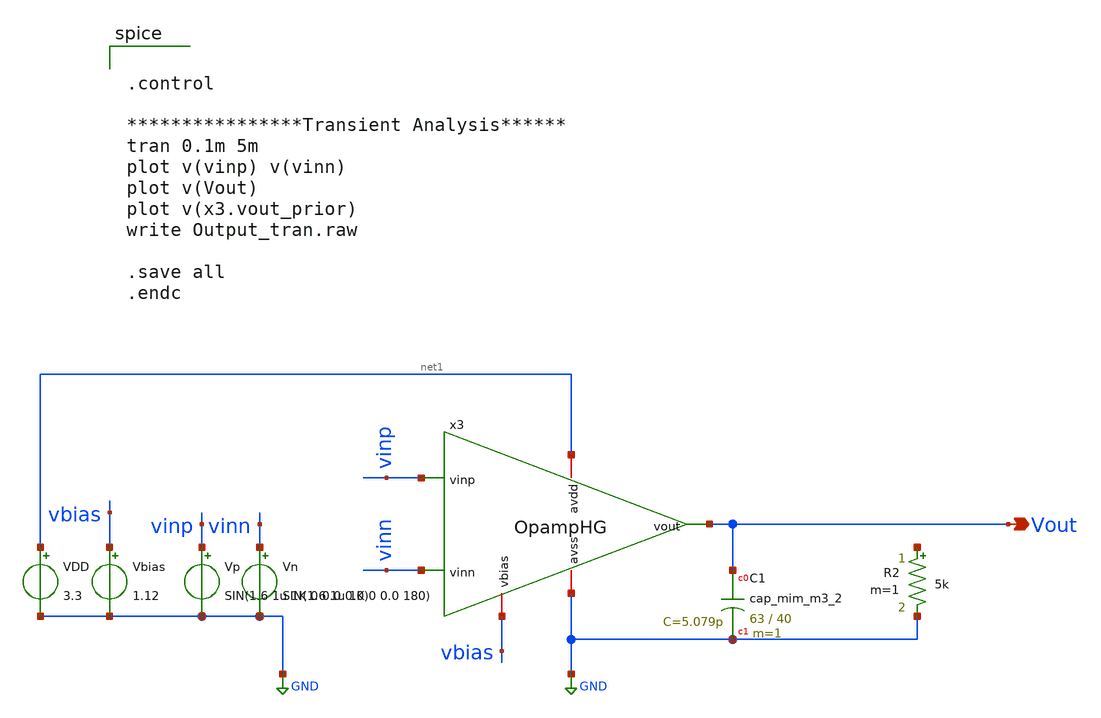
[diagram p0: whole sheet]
** sch_path: OpampHG_tran.sch
**.subckt OpampHG_tran Vout
*.opin Vout
Vp vinp GND SIN(1.6 1u 1K 0 0.0 0.0)
Vn vinn GND SIN(1.6 1u 1K 0 0.0 180)
VDD net1 GND 3.3
Vbias vbias GND 1.12
XC1 Vout GND sky130_fd_pr__cap_mim_m3_2 W=63 L=40 MF=1 m=1
x3 net1 GND vbias vinp vinn Vout OpampHG
R2 net2 GND 5k m=1
**** begin user architecture code


.control

****************Transient Analysis******
tran 0.1m 5m
plot v(vinp) v(vinn)
plot v(Vout)
plot v(x3.vout_prior)
write Output_tran.raw

.save all
.endc



** opencircuitdesign pdks install
.lib $::SKYWATER_MODELS/sky130.lib.spice tt


**** end user architecture code
**.ends

* expanding   symbol:  /foss/designs/Opamp_HG/OpampHG.sym # of pins=6
** sym_path: OpampHG.sym
** sch_path: OpampHG.sch
.subckt OpampHG avdd avss vbias vinp vinn vout
*.iopin avdd
*.iopin avss
*.iopin vbias
*.ipin vinp
*.ipin vinn
*.opin vout
XC1 net2 Vout_prior sky130_fd_pr__cap_mim_m3_1 W=13 L=9.9 MF=1 m=1
XC2 net3 vout sky130_fd_pr__cap_mim_m3_2 W=20 L=37 MF=1 m=1
XM1 net1 net2 avdd avdd sky130_fd_pr__pfet_01v8 L=0.3 W=5 nf=1 ad='int((nf+1)/2) * W/nf * 0.29' as='int((nf+2)/2) * W/nf * 0.29'
+ pd='2*int((nf+1)/2) * (W/nf + 0.29)' ps='2*int((nf+2)/2) * (W/nf + 0.29)' nrd='0.29 / W' nrs='0.29 / W'
+ sa=0 sb=0 sd=0 mult=1 m=1
XM2 net3 net2 avdd avdd sky130_fd_pr__pfet_01v8 L=0.3 W=5 nf=1 ad='int((nf+1)/2) * W/nf * 0.29' as='int((nf+2)/2) * W/nf * 0.29'
+ pd='2*int((nf+1)/2) * (W/nf + 0.29)' ps='2*int((nf+2)/2) * (W/nf + 0.29)' nrd='0.29 / W' nrs='0.29 / W'
+ sa=0 sb=0 sd=0 mult=1 m=1
XM3 net2 net2 net1 avdd sky130_fd_pr__pfet_01v8 L=0.3 W=5 nf=1 ad='int((nf+1)/2) * W/nf * 0.29' as='int((nf+2)/2) * W/nf * 0.29'
+ pd='2*int((nf+1)/2) * (W/nf + 0.29)' ps='2*int((nf+2)/2) * (W/nf + 0.29)' nrd='0.29 / W' nrs='0.29 / W'
+ sa=0 sb=0 sd=0 mult=1 m=1
XM4 net5 net2 net3 avdd sky130_fd_pr__pfet_01v8 L=0.3 W=5 nf=1 ad='int((nf+1)/2) * W/nf * 0.29' as='int((nf+2)/2) * W/nf * 0.29'
+ pd='2*int((nf+1)/2) * (W/nf + 0.29)' ps='2*int((nf+2)/2) * (W/nf + 0.29)' nrd='0.29 / W' nrs='0.29 / W'
+ sa=0 sb=0 sd=0 mult=1 m=1
XM5 net7 net6 avdd avdd sky130_fd_pr__pfet_01v8 L=0.3 W=5 nf=1 ad='int((nf+1)/2) * W/nf * 0.29' as='int((nf+2)/2) * W/nf * 0.29'
+ pd='2*int((nf+1)/2) * (W/nf + 0.29)' ps='2*int((nf+2)/2) * (W/nf + 0.29)' nrd='0.29 / W' nrs='0.29 / W'
+ sa=0 sb=0 sd=0 mult=1 m=1
XM6 net8 net6 avdd avdd sky130_fd_pr__pfet_01v8 L=0.3 W=5 nf=1 ad='int((nf+1)/2) * W/nf * 0.29' as='int((nf+2)/2) * W/nf * 0.29'
+ pd='2*int((nf+1)/2) * (W/nf + 0.29)' ps='2*int((nf+2)/2) * (W/nf + 0.29)' nrd='0.29 / W' nrs='0.29 / W'
+ sa=0 sb=0 sd=0 mult=1 m=1
XM7 net6 net6 net7 avdd sky130_fd_pr__pfet_01v8 L=0.3 W=5 nf=1 ad='int((nf+1)/2) * W/nf * 0.29' as='int((nf+2)/2) * W/nf * 0.29'
+ pd='2*int((nf+1)/2) * (W/nf + 0.29)' ps='2*int((nf+2)/2) * (W/nf + 0.29)' nrd='0.29 / W' nrs='0.29 / W'
+ sa=0 sb=0 sd=0 mult=1 m=1
XM8 Vout_prior net6 net8 avdd sky130_fd_pr__pfet_01v8 L=0.3 W=5 nf=1 ad='int((nf+1)/2) * W/nf * 0.29'
+ as='int((nf+2)/2) * W/nf * 0.29' pd='2*int((nf+1)/2) * (W/nf + 0.29)' ps='2*int((nf+2)/2) * (W/nf + 0.29)'
+ nrd='0.29 / W' nrs='0.29 / W' sa=0 sb=0 sd=0 mult=1 m=1
XM9 net11 Vout_prior avdd avdd sky130_fd_pr__pfet_01v8 L=0.3 W=50 nf=1 ad='int((nf+1)/2) * W/nf * 0.29'
+ as='int((nf+2)/2) * W/nf * 0.29' pd='2*int((nf+1)/2) * (W/nf + 0.29)' ps='2*int((nf+2)/2) * (W/nf + 0.29)'
+ nrd='0.29 / W' nrs='0.29 / W' sa=0 sb=0 sd=0 mult=1 m=1
XM10 vout Vout_prior net11 avdd sky130_fd_pr__pfet_01v8 L=0.3 W=50 nf=1 ad='int((nf+1)/2) * W/nf * 0.29'
+ as='int((nf+2)/2) * W/nf * 0.29' pd='2*int((nf+1)/2) * (W/nf + 0.29)' ps='2*int((nf+2)/2) * (W/nf + 0.29)'
+ nrd='0.29 / W' nrs='0.29 / W' sa=0 sb=0 sd=0 mult=1 m=1
XM11 net2 vinn net4 avss sky130_fd_pr__nfet_01v8 L=2 W=5 nf=1 ad='int((nf+1)/2) * W/nf * 0.29' as='int((nf+2)/2) * W/nf * 0.29'
+ pd='2*int((nf+1)/2) * (W/nf + 0.29)' ps='2*int((nf+2)/2) * (W/nf + 0.29)' nrd='0.29 / W' nrs='0.29 / W'
+ sa=0 sb=0 sd=0 mult=1 m=1
XM12 net5 vinp net4 avss sky130_fd_pr__nfet_01v8 L=2 W=5 nf=1 ad='int((nf+1)/2) * W/nf * 0.29' as='int((nf+2)/2) * W/nf * 0.29'
+ pd='2*int((nf+1)/2) * (W/nf + 0.29)' ps='2*int((nf+2)/2) * (W/nf + 0.29)' nrd='0.29 / W' nrs='0.29 / W'
+ sa=0 sb=0 sd=0 mult=1 m=1
XM13 net6 net5 net10 avss sky130_fd_pr__nfet_01v8 L=2 W=5 nf=1 ad='int((nf+1)/2) * W/nf * 0.29' as='int((nf+2)/2) * W/nf * 0.29'
+ pd='2*int((nf+1)/2) * (W/nf + 0.29)' ps='2*int((nf+2)/2) * (W/nf + 0.29)' nrd='0.29 / W' nrs='0.29 / W'
+ sa=0 sb=0 sd=0 mult=1 m=1
XM14 Vout_prior net2 net9 avss sky130_fd_pr__nfet_01v8 L=2 W=5 nf=1 ad='int((nf+1)/2) * W/nf * 0.29'
+ as='int((nf+2)/2) * W/nf * 0.29' pd='2*int((nf+1)/2) * (W/nf + 0.29)' ps='2*int((nf+2)/2) * (W/nf + 0.29)'
+ nrd='0.29 / W' nrs='0.29 / W' sa=0 sb=0 sd=0 mult=1 m=1
XM15 net4 vbias avss avss sky130_fd_pr__nfet_01v8 L=0.6 W=2.6 nf=1 ad='int((nf+1)/2) * W/nf * 0.29' as='int((nf+2)/2) * W/nf * 0.29'
+ pd='2*int((nf+1)/2) * (W/nf + 0.29)' ps='2*int((nf+2)/2) * (W/nf + 0.29)' nrd='0.29 / W' nrs='0.29 / W'
+ sa=0 sb=0 sd=0 mult=1 m=1
XM16 net4 vbias avss avss sky130_fd_pr__nfet_01v8 L=0.6 W=2.6 nf=1 ad='int((nf+1)/2) * W/nf * 0.29' as='int((nf+2)/2) * W/nf * 0.29'
+ pd='2*int((nf+1)/2) * (W/nf + 0.29)' ps='2*int((nf+2)/2) * (W/nf + 0.29)' nrd='0.29 / W' nrs='0.29 / W'
+ sa=0 sb=0 sd=0 mult=1 m=1
XM17 net10 vbias avss avss sky130_fd_pr__nfet_01v8 L=0.6 W=2.6 nf=1 ad='int((nf+1)/2) * W/nf * 0.29'
+ as='int((nf+2)/2) * W/nf * 0.29' pd='2*int((nf+1)/2) * (W/nf + 0.29)' ps='2*int((nf+2)/2) * (W/nf + 0.29)'
+ nrd='0.29 / W' nrs='0.29 / W' sa=0 sb=0 sd=0 mult=1 m=1
XM18 net9 vbias avss avss sky130_fd_pr__nfet_01v8 L=0.6 W=2.6 nf=1 ad='int((nf+1)/2) * W/nf * 0.29' as='int((nf+2)/2) * W/nf * 0.29'
+ pd='2*int((nf+1)/2) * (W/nf + 0.29)' ps='2*int((nf+2)/2) * (W/nf + 0.29)' nrd='0.29 / W' nrs='0.29 / W'
+ sa=0 sb=0 sd=0 mult=1 m=1
XM19 vout vbias avss avss sky130_fd_pr__nfet_01v8 L=0.6 W=20.4 nf=1 ad='int((nf+1)/2) * W/nf * 0.29'
+ as='int((nf+2)/2) * W/nf * 0.29' pd='2*int((nf+1)/2) * (W/nf + 0.29)' ps='2*int((nf+2)/2) * (W/nf + 0.29)'
+ nrd='0.29 / W' nrs='0.29 / W' sa=0 sb=0 sd=0 mult=1 m=1
.ends

.GLOBAL GND
.end
